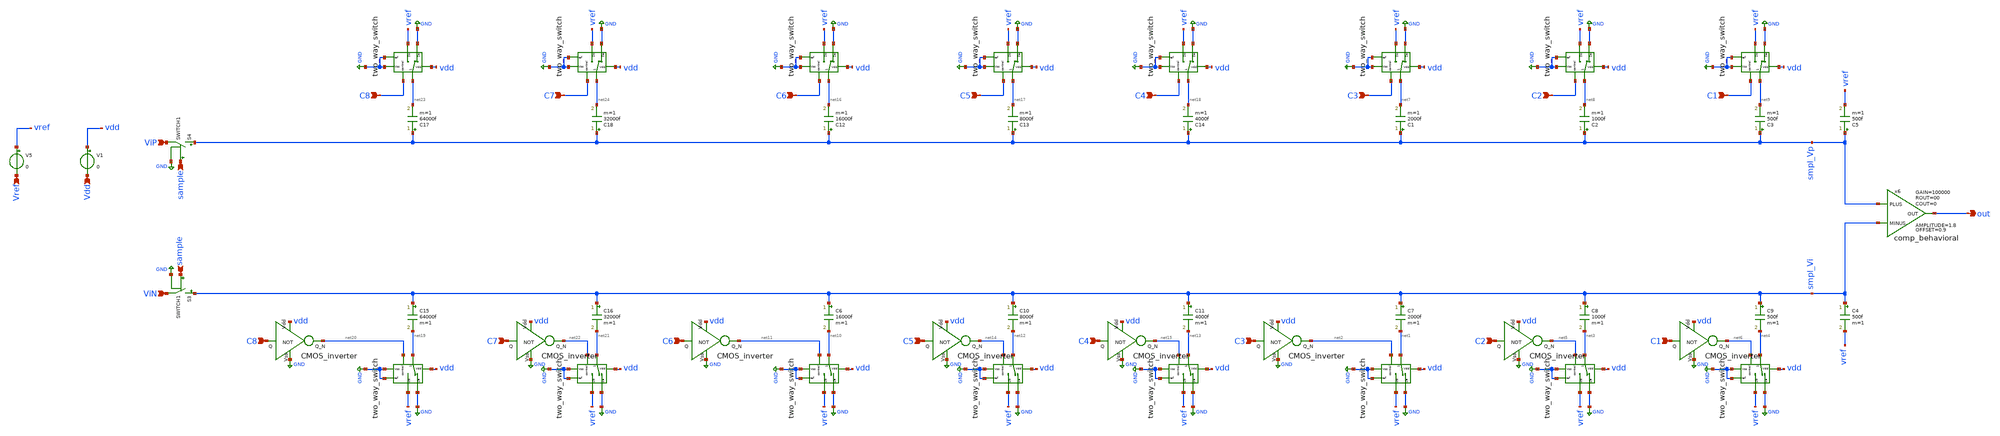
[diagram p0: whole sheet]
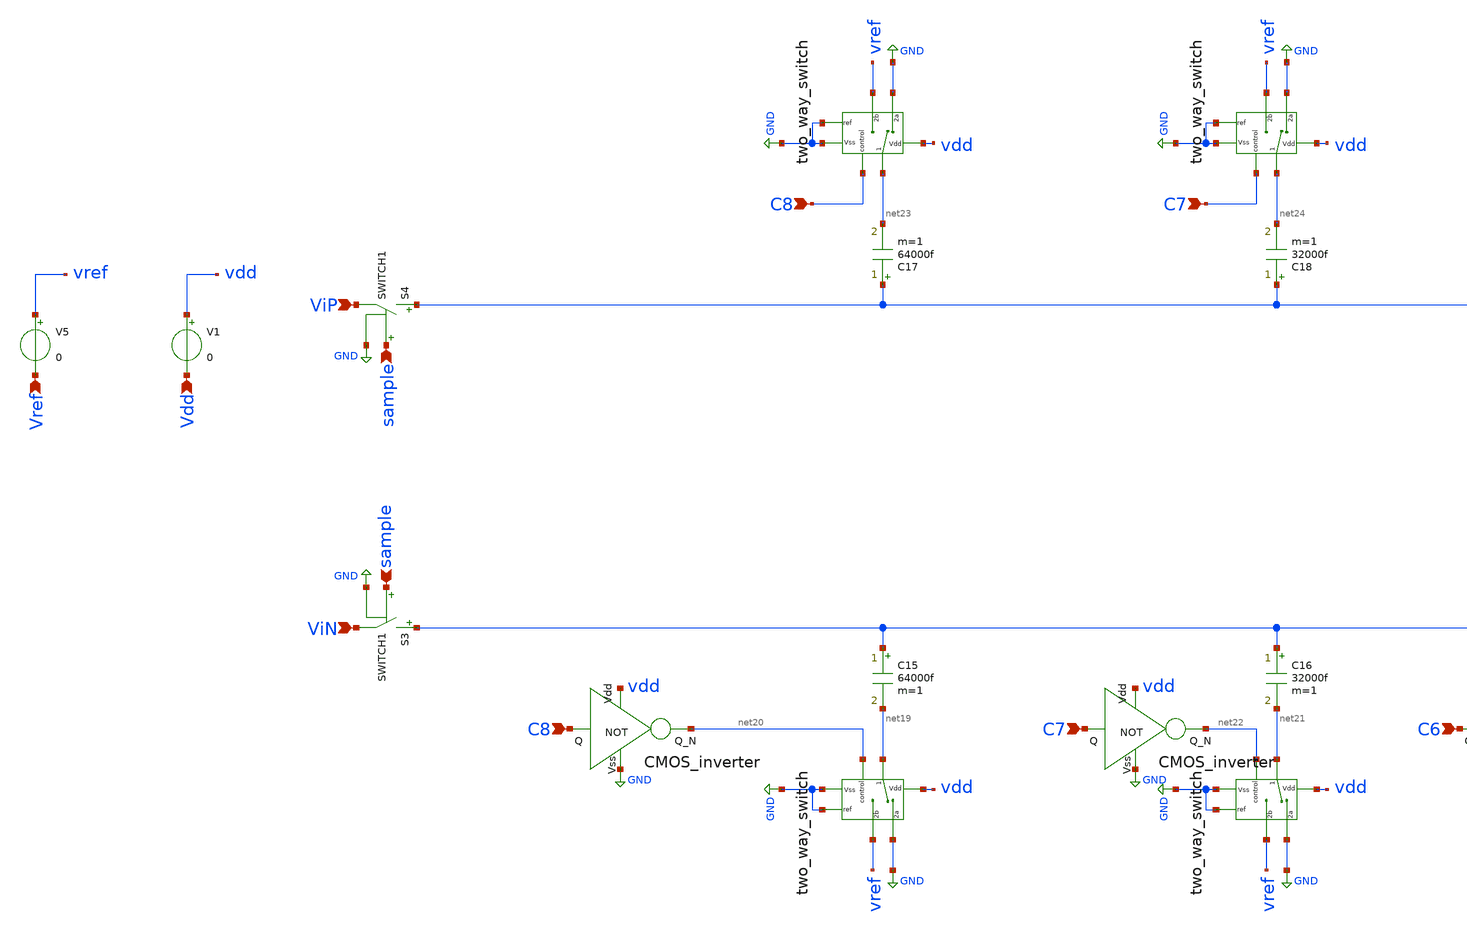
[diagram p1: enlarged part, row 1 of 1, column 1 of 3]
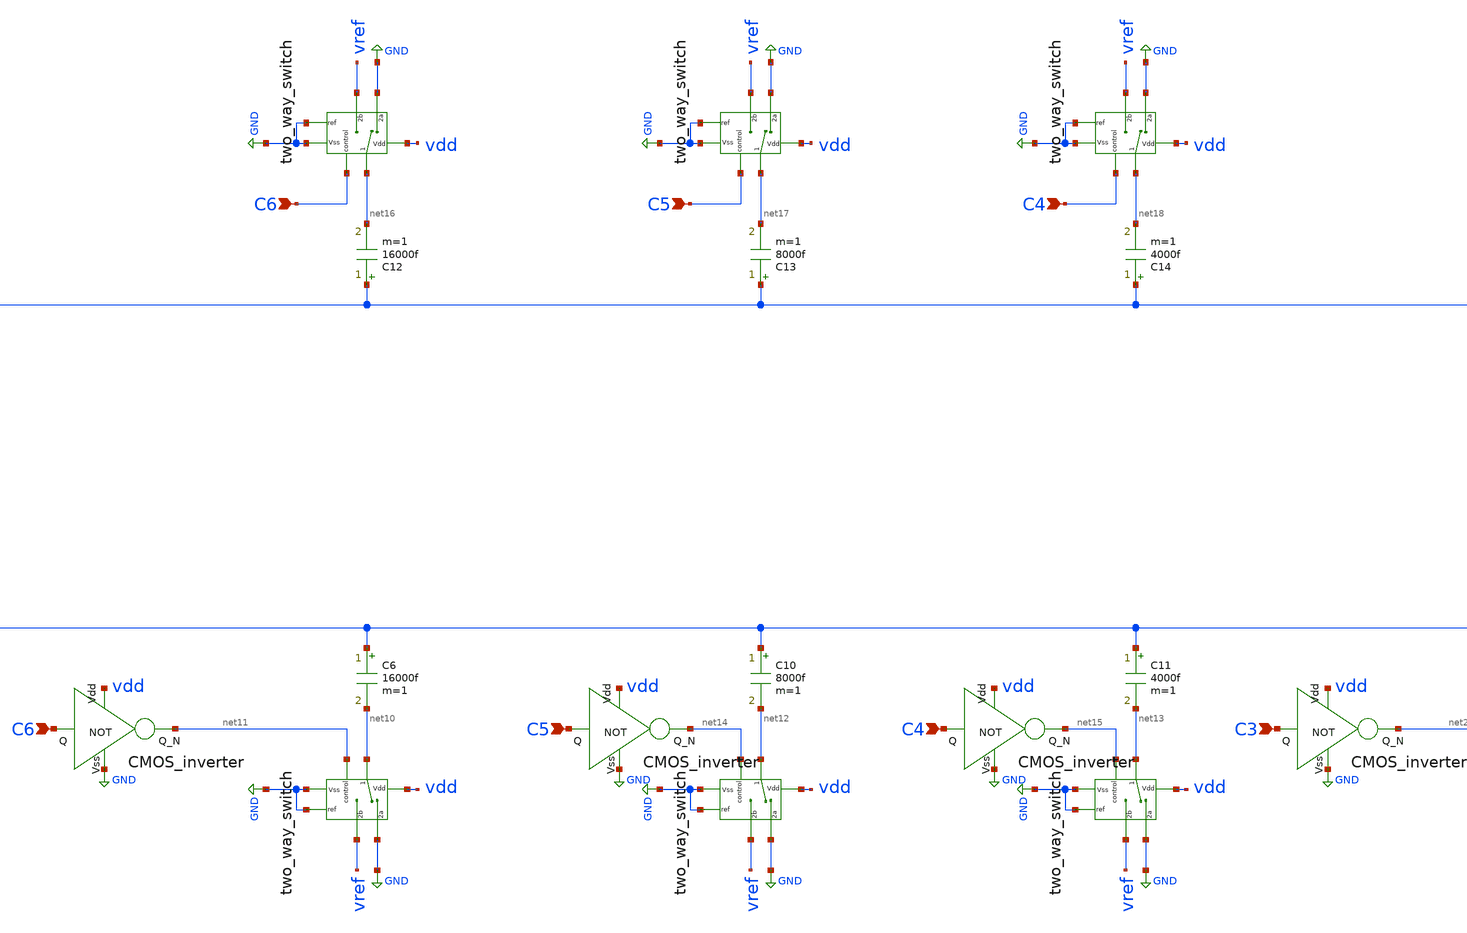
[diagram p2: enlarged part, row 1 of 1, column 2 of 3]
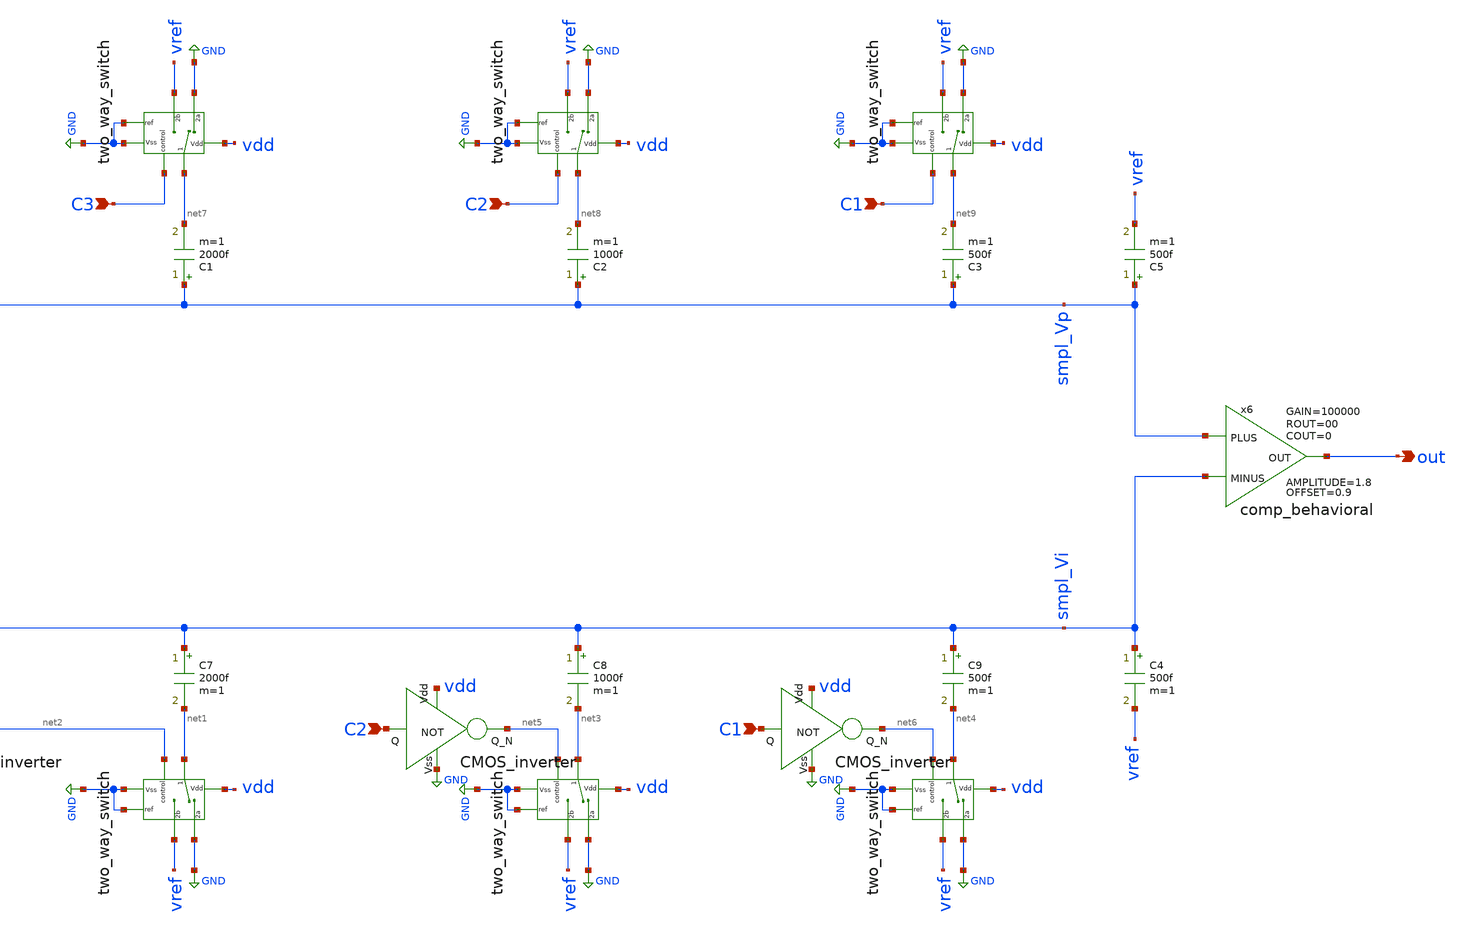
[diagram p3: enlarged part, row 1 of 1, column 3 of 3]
** sch_path: Behavioral_model/diff_mode_behavioral_no_tb.sch
**.subckt diff_mode_behavioral_no_tb ViP ViN C8 C7 C6 C5 C4 C3 C2 C1 C8 C7 C6 C5 C4 C3 C2 C1 sample
*+ sample Vref Vdd out
*.ipin ViP
*.ipin ViN
*.ipin C8
*.ipin C7
*.ipin C6
*.ipin C5
*.ipin C4
*.ipin C3
*.ipin C2
*.ipin C1
*.ipin C8
*.ipin C7
*.ipin C6
*.ipin C5
*.ipin C4
*.ipin C3
*.ipin C2
*.ipin C1
*.ipin sample
*.ipin sample
*.ipin Vref
*.ipin Vdd
*.opin out
S3 smpl_Vi ViN sample GND SWITCH1
C7 smpl_Vi net1 2000f m=1
x7 net1 vdd net2 GND GND vref GND two_way_switch
C8 smpl_Vi net3 1000f m=1
C9 smpl_Vi net4 500f m=1
x1 net3 vdd net5 GND GND vref GND two_way_switch
x2 net4 vdd net6 GND GND vref GND two_way_switch
S4 smpl_Vp ViP sample GND SWITCH1
C1 smpl_Vp net7 2000f m=1
x3 net7 vdd C3 GND GND vref GND two_way_switch
C2 smpl_Vp net8 1000f m=1
C3 smpl_Vp net9 500f m=1
x4 net8 vdd C2 GND GND vref GND two_way_switch
x5 net9 vdd C1 GND GND vref GND two_way_switch
x6 smpl_Vp smpl_Vi out comp_behavioral OFFSET=0.9 AMPLITUDE=1.8 GAIN=100000 ROUT=00 COUT=0
C4 smpl_Vi vref 500f m=1
C5 smpl_Vp vref 500f m=1
x8 vdd C3 net2 GND CMOS_inverter
x9 vdd C2 net5 GND CMOS_inverter
x10 vdd C1 net6 GND CMOS_inverter
C6 smpl_Vi net10 16000f m=1
x11 net10 vdd net11 GND GND vref GND two_way_switch
C10 smpl_Vi net12 8000f m=1
C11 smpl_Vi net13 4000f m=1
x12 net12 vdd net14 GND GND vref GND two_way_switch
x13 net13 vdd net15 GND GND vref GND two_way_switch
C12 smpl_Vp net16 16000f m=1
x14 net16 vdd C6 GND GND vref GND two_way_switch
C13 smpl_Vp net17 8000f m=1
C14 smpl_Vp net18 4000f m=1
x15 net17 vdd C5 GND GND vref GND two_way_switch
x16 net18 vdd C4 GND GND vref GND two_way_switch
x17 vdd C6 net11 GND CMOS_inverter
x18 vdd C5 net14 GND CMOS_inverter
x19 vdd C4 net15 GND CMOS_inverter
C15 smpl_Vi net19 64000f m=1
x20 net19 vdd net20 GND GND vref GND two_way_switch
C16 smpl_Vi net21 32000f m=1
x21 net21 vdd net22 GND GND vref GND two_way_switch
C17 smpl_Vp net23 64000f m=1
x22 net23 vdd C8 GND GND vref GND two_way_switch
C18 smpl_Vp net24 32000f m=1
x23 net24 vdd C7 GND GND vref GND two_way_switch
x24 vdd C8 net20 GND CMOS_inverter
x25 vdd C7 net22 GND CMOS_inverter
V5 vref Vref 0
V1 vdd Vdd 0
**** begin user architecture code

.lib /usr/local/share/pdk/sky130A/libs.tech/ngspice/sky130.lib.spice tt


.model switch1 sw vt=0.1 vh=0 ron=1m roff=100G

**** end user architecture code
**.ends

* expanding   symbol:  two_way_switch.sym # of pins=7
** sym_path: Behavioral_model/two_way_switch.sym
** sch_path: Behavioral_model/two_way_switch.sch
.subckt two_way_switch 1 Vdd control ref 2a 2b Vss
*.iopin 2b
*.iopin 2a
*.ipin ref
*.iopin 1
*.ipin Vdd
*.ipin Vss
*.ipin control
S1 1 2a control ref SWITCH1
S2 1 2b net1 ref SWITCH1
x1 Vdd control net1 Vss CMOS_inverter
.ends


* expanding   symbol:  comp_behavioral.sym # of pins=3
** sym_path: Behavioral_model/comp_behavioral.sym
** sch_path: Behavioral_model/comp_behavioral.sch
.subckt comp_behavioral PLUS MINUS OUT  OFFSET=0.9 AMPLITUDE=0.9 GAIN=100000 ROUT=00 COUT=0
*.ipin PLUS
*.ipin MINUS
*.opin OUT
B1 IOUT 0 V = {OFFSET + AMPLITUDE/2*(tanh(V(IPLUS,IMINUS)*GAIN*2/AMPLITUDE))}
V1 IPLUS PLUS 3
V2 IMINUS MINUS 3
R1 OUT IOUT {ROUT} m=1
C3 OUT 0 {COUT} m=1
.ends


* expanding   symbol:  CMOS_inverter.sym # of pins=4
** sym_path: Behavioral_model/CMOS_inverter.sym
** sch_path: Behavioral_model/CMOS_inverter.sch
.subckt CMOS_inverter Vdd Q Q_N Vss
*.ipin Q
*.ipin Vdd
*.ipin Vss
*.opin Q_N
XM1 Q_N Q Vss Vss sky130_fd_pr__nfet_01v8 L=0.15 W=1 nf=1 ad='int((nf+1)/2) * W/nf * 0.29' as='int((nf+2)/2) * W/nf * 0.29'
+ pd='2*int((nf+1)/2) * (W/nf + 0.29)' ps='2*int((nf+2)/2) * (W/nf + 0.29)' nrd='0.29 / W' nrs='0.29 / W'
+ sa=0 sb=0 sd=0 mult=1 m=1
XM3 Q_N Q Vdd Vdd sky130_fd_pr__pfet_01v8 L=0.15 W=1 nf=1 ad='int((nf+1)/2) * W/nf * 0.29' as='int((nf+2)/2) * W/nf * 0.29'
+ pd='2*int((nf+1)/2) * (W/nf + 0.29)' ps='2*int((nf+2)/2) * (W/nf + 0.29)' nrd='0.29 / W' nrs='0.29 / W'
+ sa=0 sb=0 sd=0 mult=1 m=1
.ends

.GLOBAL GND
.end
